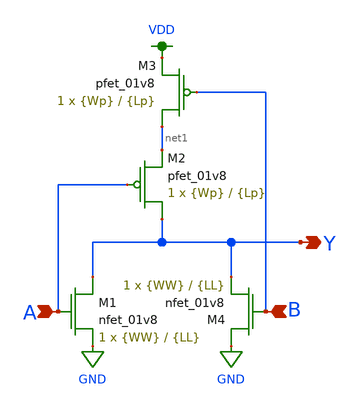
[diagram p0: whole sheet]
** sch_path: schematic/nor2.sch
**.subckt nor2 A B Y
*.ipin A
*.ipin B
*.opin Y
XM1 Y A GND GND sky130_fd_pr__nfet_01v8 L={LL} W={WW} nf=1 ad='int((nf+1)/2) * W/nf * 0.29' as='int((nf+2)/2) * W/nf * 0.29'
+ pd='2*int((nf+1)/2) * (W/nf + 0.29)' ps='2*int((nf+2)/2) * (W/nf + 0.29)' nrd='0.29 / W' nrs='0.29 / W'
+ sa=0 sb=0 sd=0 mult=1 m=1
XM2 Y A net1 VDD sky130_fd_pr__pfet_01v8 L={Lp} W={Wp} nf=1 ad='int((nf+1)/2) * W/nf * 0.29' as='int((nf+2)/2) * W/nf * 0.29'
+ pd='2*int((nf+1)/2) * (W/nf + 0.29)' ps='2*int((nf+2)/2) * (W/nf + 0.29)' nrd='0.29 / W' nrs='0.29 / W'
+ sa=0 sb=0 sd=0 mult=1 m=1
XM3 net1 B VDD VDD sky130_fd_pr__pfet_01v8 L={Lp} W={Wp} nf=1 ad='int((nf+1)/2) * W/nf * 0.29' as='int((nf+2)/2) * W/nf * 0.29'
+ pd='2*int((nf+1)/2) * (W/nf + 0.29)' ps='2*int((nf+2)/2) * (W/nf + 0.29)' nrd='0.29 / W' nrs='0.29 / W'
+ sa=0 sb=0 sd=0 mult=1 m=1
XM4 GND B Y GND sky130_fd_pr__nfet_01v8 L={LL} W={WW} nf=1 ad='int((nf+1)/2) * W/nf * 0.29' as='int((nf+2)/2) * W/nf * 0.29'
+ pd='2*int((nf+1)/2) * (W/nf + 0.29)' ps='2*int((nf+2)/2) * (W/nf + 0.29)' nrd='0.29 / W' nrs='0.29 / W'
+ sa=0 sb=0 sd=0 mult=1 m=1
**.ends
.GLOBAL GND
.GLOBAL VDD
.end
